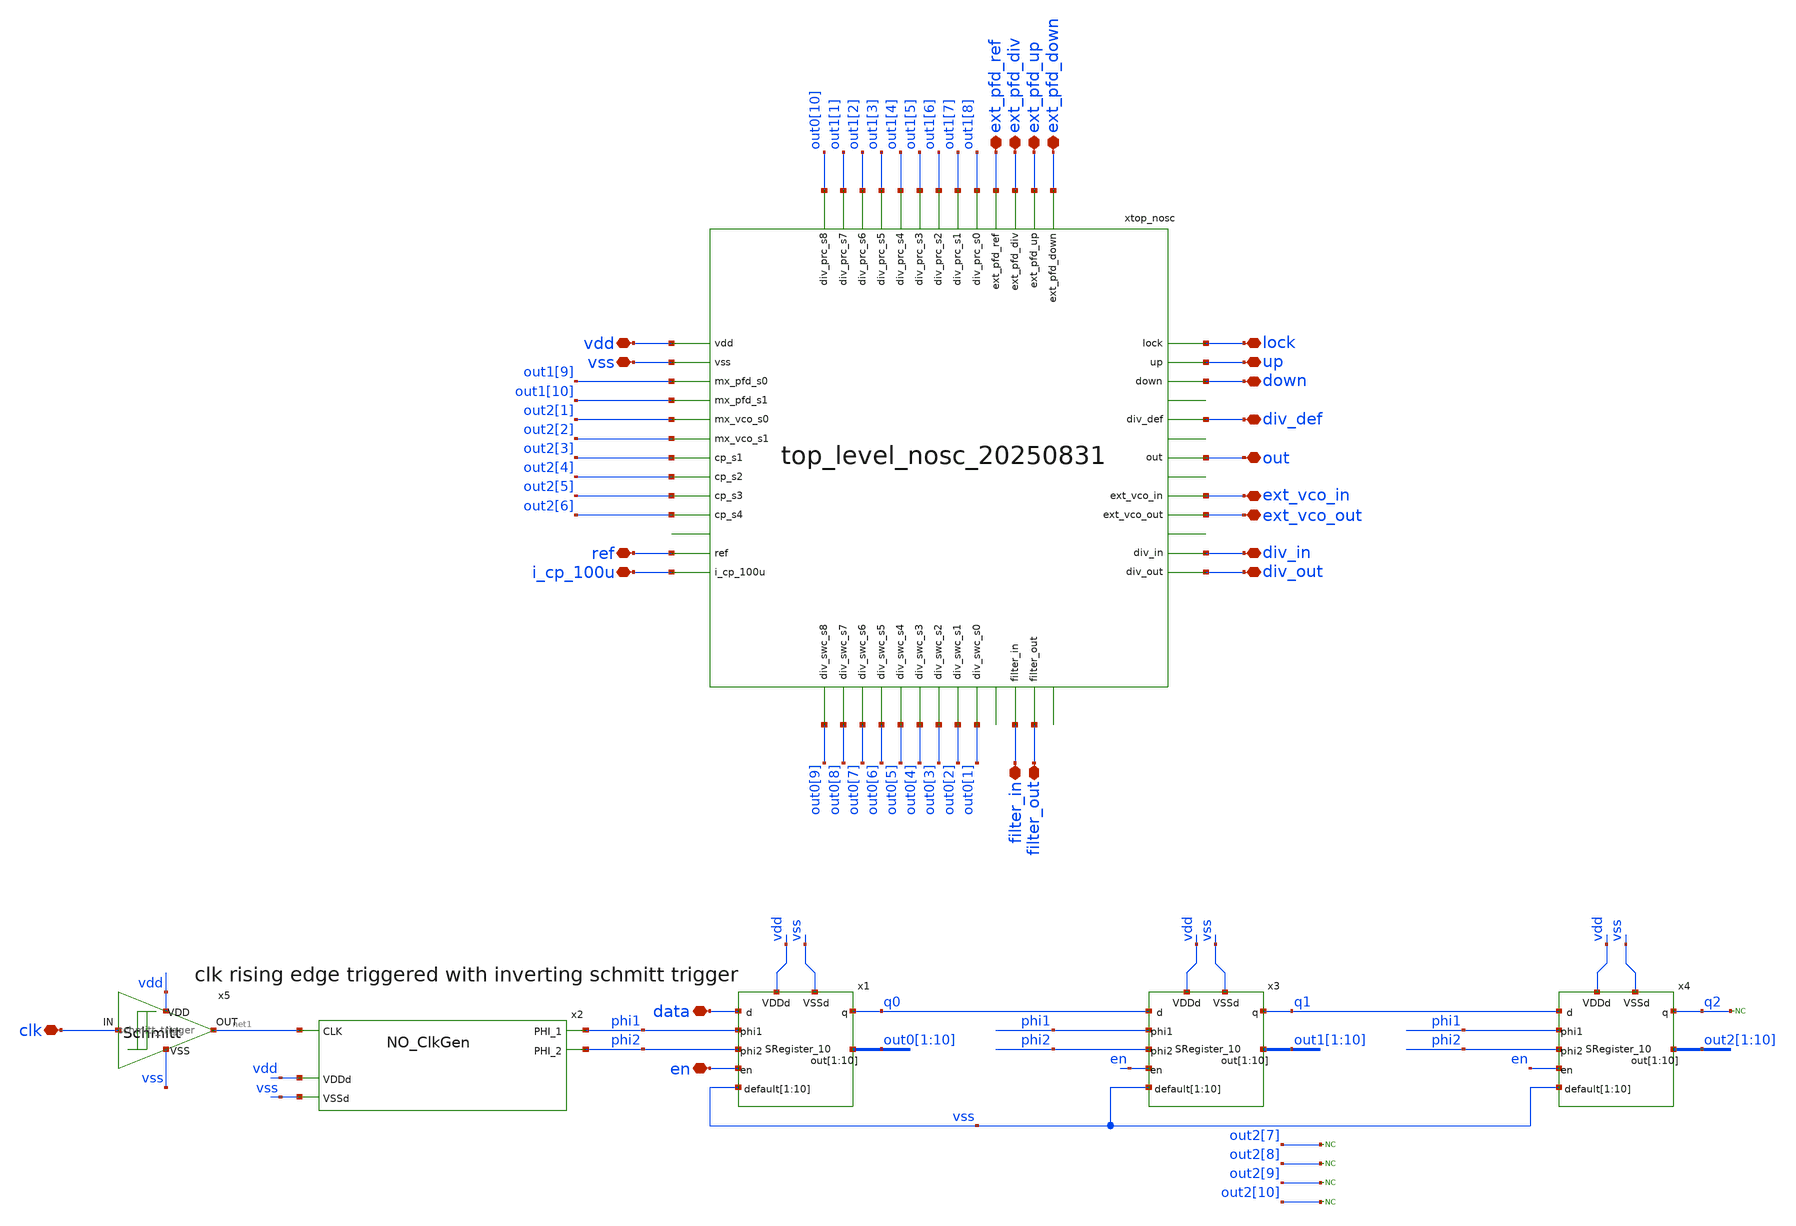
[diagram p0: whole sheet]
** sch_path: designs/libs/top_level/top_level_20250831/top_level_sc_20250831/top_level_sc_20250831.sch
**.subckt top_level_sc_20250831 vdd vss ref i_cp_100u filter_in filter_out ext_pfd_ref ext_pfd_up
*+ ext_pfd_down ext_pfd_div up down out lock ext_vco_out ext_vco_in div_out div_in div_def clk data en
*.iopin vdd
*.iopin vss
*.iopin ref
*.iopin i_cp_100u
*.iopin filter_in
*.iopin filter_out
*.iopin ext_pfd_ref
*.iopin ext_pfd_up
*.iopin ext_pfd_down
*.iopin ext_pfd_div
*.iopin up
*.iopin down
*.iopin out
*.iopin lock
*.iopin ext_vco_out
*.iopin ext_vco_in
*.iopin div_out
*.iopin div_in
*.iopin div_def
*.iopin clk
*.iopin data
*.iopin en
xtop_nosc vdd vss out1[9] out1[10] out2[1] out2[2] out0[9] out2[3] out2[4] out2[5] out2[6] out0[8]
+ out0[7] out0[6] out0[5] out0[4] out0[3] out0[2] out0[1] out0[10] out1[1] out1[2] out1[3] out1[4] out1[5]
+ out1[6] out1[7] out1[8] ref i_cp_100u ext_pfd_ref ext_pfd_div ext_pfd_up ext_pfd_down lock up down
+ filter_out ext_vco_in div_in div_out out filter_in ext_vco_out div_def top_level_nosc_20250831
x2 phi2 net1 phi1 vdd vss NO_ClkGen
x1 vdd vss phi1 phi2 en vss vss vss vss vss vss vss vss vss vss data q0 out0[1] out0[2] out0[3]
+ out0[4] out0[5] out0[6] out0[7] out0[8] out0[9] out0[10] SRegister_10
x3 vdd vss phi1 phi2 en vss vss vss vss vss vss vss vss vss vss q0 q1 out1[1] out1[2] out1[3]
+ out1[4] out1[5] out1[6] out1[7] out1[8] out1[9] out1[10] SRegister_10
x4 vdd vss phi1 phi2 en vss vss vss vss vss vss vss vss vss vss q1 q2 out2[1] out2[2] out2[3]
+ out2[4] out2[5] out2[6] out2[7] out2[8] out2[9] out2[10] SRegister_10
* noconn q2
x5 clk net1 vdd vss schmitt_trigger
* noconn out2[7]
* noconn out2[8]
* noconn out2[9]
* noconn out2[10]
**.ends
.end
